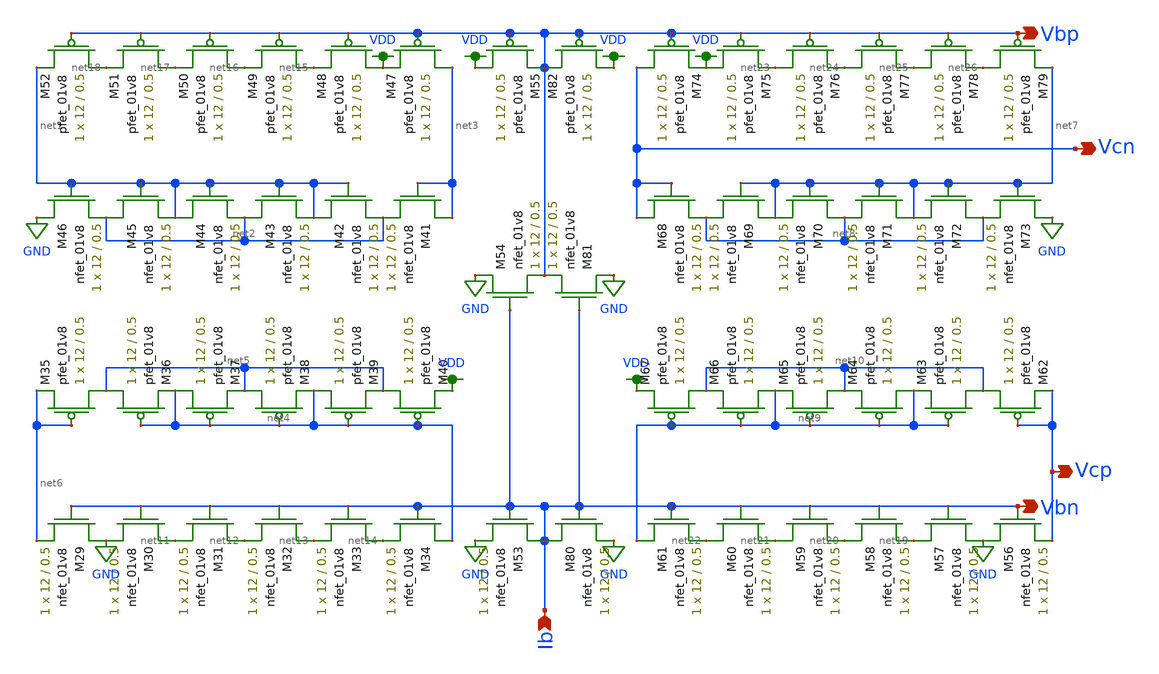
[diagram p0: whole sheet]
** sch_path: mp3/schematics/bias_lds.sch
**.subckt bias_lds Vbp Vbn Vcp Vcn Ib
*.opin Vbp
*.opin Vbn
*.opin Vcp
*.opin Vcn
*.ipin Ib
XM29 GND Vbn net6 GND sky130_fd_pr__nfet_01v8 L=0.5 W=12 nf=1 ad='int((nf+1)/2) * W/nf * 0.29' as='int((nf+2)/2) * W/nf * 0.29'
+ pd='2*int((nf+1)/2) * (W/nf + 0.29)' ps='2*int((nf+2)/2) * (W/nf + 0.29)' nrd='0.29 / W' nrs='0.29 / W'
+ sa=0 sb=0 sd=0 mult=1 m=1
XM30 net11 Vbn GND GND sky130_fd_pr__nfet_01v8 L=0.5 W=12 nf=1 ad='int((nf+1)/2) * W/nf * 0.29' as='int((nf+2)/2) * W/nf * 0.29'
+ pd='2*int((nf+1)/2) * (W/nf + 0.29)' ps='2*int((nf+2)/2) * (W/nf + 0.29)' nrd='0.29 / W' nrs='0.29 / W'
+ sa=0 sb=0 sd=0 mult=1 m=1
XM31 net12 Vbn net11 GND sky130_fd_pr__nfet_01v8 L=0.5 W=12 nf=1 ad='int((nf+1)/2) * W/nf * 0.29' as='int((nf+2)/2) * W/nf * 0.29'
+ pd='2*int((nf+1)/2) * (W/nf + 0.29)' ps='2*int((nf+2)/2) * (W/nf + 0.29)' nrd='0.29 / W' nrs='0.29 / W'
+ sa=0 sb=0 sd=0 mult=1 m=1
XM32 net13 Vbn net12 GND sky130_fd_pr__nfet_01v8 L=0.5 W=12 nf=1 ad='int((nf+1)/2) * W/nf * 0.29' as='int((nf+2)/2) * W/nf * 0.29'
+ pd='2*int((nf+1)/2) * (W/nf + 0.29)' ps='2*int((nf+2)/2) * (W/nf + 0.29)' nrd='0.29 / W' nrs='0.29 / W'
+ sa=0 sb=0 sd=0 mult=1 m=1
XM33 net14 Vbn net13 GND sky130_fd_pr__nfet_01v8 L=0.5 W=12 nf=1 ad='int((nf+1)/2) * W/nf * 0.29' as='int((nf+2)/2) * W/nf * 0.29'
+ pd='2*int((nf+1)/2) * (W/nf + 0.29)' ps='2*int((nf+2)/2) * (W/nf + 0.29)' nrd='0.29 / W' nrs='0.29 / W'
+ sa=0 sb=0 sd=0 mult=1 m=1
XM34 net4 Vbn net14 GND sky130_fd_pr__nfet_01v8 L=0.5 W=12 nf=1 ad='int((nf+1)/2) * W/nf * 0.29' as='int((nf+2)/2) * W/nf * 0.29'
+ pd='2*int((nf+1)/2) * (W/nf + 0.29)' ps='2*int((nf+2)/2) * (W/nf + 0.29)' nrd='0.29 / W' nrs='0.29 / W'
+ sa=0 sb=0 sd=0 mult=1 m=1
XM35 net5 net6 net6 VDD sky130_fd_pr__pfet_01v8 L=0.5 W=12 nf=1 ad='int((nf+1)/2) * W/nf * 0.29' as='int((nf+2)/2) * W/nf * 0.29'
+ pd='2*int((nf+1)/2) * (W/nf + 0.29)' ps='2*int((nf+2)/2) * (W/nf + 0.29)' nrd='0.29 / W' nrs='0.29 / W'
+ sa=0 sb=0 sd=0 mult=1 m=1
XM36 net5 net4 net4 VDD sky130_fd_pr__pfet_01v8 L=0.5 W=12 nf=1 ad='int((nf+1)/2) * W/nf * 0.29' as='int((nf+2)/2) * W/nf * 0.29'
+ pd='2*int((nf+1)/2) * (W/nf + 0.29)' ps='2*int((nf+2)/2) * (W/nf + 0.29)' nrd='0.29 / W' nrs='0.29 / W'
+ sa=0 sb=0 sd=0 mult=1 m=1
XM37 net4 net4 net5 VDD sky130_fd_pr__pfet_01v8 L=0.5 W=12 nf=1 ad='int((nf+1)/2) * W/nf * 0.29' as='int((nf+2)/2) * W/nf * 0.29'
+ pd='2*int((nf+1)/2) * (W/nf + 0.29)' ps='2*int((nf+2)/2) * (W/nf + 0.29)' nrd='0.29 / W' nrs='0.29 / W'
+ sa=0 sb=0 sd=0 mult=1 m=1
XM38 net5 net4 net4 VDD sky130_fd_pr__pfet_01v8 L=0.5 W=12 nf=1 ad='int((nf+1)/2) * W/nf * 0.29' as='int((nf+2)/2) * W/nf * 0.29'
+ pd='2*int((nf+1)/2) * (W/nf + 0.29)' ps='2*int((nf+2)/2) * (W/nf + 0.29)' nrd='0.29 / W' nrs='0.29 / W'
+ sa=0 sb=0 sd=0 mult=1 m=1
XM39 net4 net4 net5 VDD sky130_fd_pr__pfet_01v8 L=0.5 W=12 nf=1 ad='int((nf+1)/2) * W/nf * 0.29' as='int((nf+2)/2) * W/nf * 0.29'
+ pd='2*int((nf+1)/2) * (W/nf + 0.29)' ps='2*int((nf+2)/2) * (W/nf + 0.29)' nrd='0.29 / W' nrs='0.29 / W'
+ sa=0 sb=0 sd=0 mult=1 m=1
XM40 net5 net4 VDD VDD sky130_fd_pr__pfet_01v8 L=0.5 W=12 nf=1 ad='int((nf+1)/2) * W/nf * 0.29' as='int((nf+2)/2) * W/nf * 0.29'
+ pd='2*int((nf+1)/2) * (W/nf + 0.29)' ps='2*int((nf+2)/2) * (W/nf + 0.29)' nrd='0.29 / W' nrs='0.29 / W'
+ sa=0 sb=0 sd=0 mult=1 m=1
XM41 net3 net3 net2 GND sky130_fd_pr__nfet_01v8 L=0.5 W=12 nf=1 ad='int((nf+1)/2) * W/nf * 0.29' as='int((nf+2)/2) * W/nf * 0.29'
+ pd='2*int((nf+1)/2) * (W/nf + 0.29)' ps='2*int((nf+2)/2) * (W/nf + 0.29)' nrd='0.29 / W' nrs='0.29 / W'
+ sa=0 sb=0 sd=0 mult=1 m=1
XM42 net1 net1 net2 GND sky130_fd_pr__nfet_01v8 L=0.5 W=12 nf=1 ad='int((nf+1)/2) * W/nf * 0.29' as='int((nf+2)/2) * W/nf * 0.29'
+ pd='2*int((nf+1)/2) * (W/nf + 0.29)' ps='2*int((nf+2)/2) * (W/nf + 0.29)' nrd='0.29 / W' nrs='0.29 / W'
+ sa=0 sb=0 sd=0 mult=1 m=1
XM43 net2 net1 net1 GND sky130_fd_pr__nfet_01v8 L=0.5 W=12 nf=1 ad='int((nf+1)/2) * W/nf * 0.29' as='int((nf+2)/2) * W/nf * 0.29'
+ pd='2*int((nf+1)/2) * (W/nf + 0.29)' ps='2*int((nf+2)/2) * (W/nf + 0.29)' nrd='0.29 / W' nrs='0.29 / W'
+ sa=0 sb=0 sd=0 mult=1 m=1
XM44 net1 net1 net2 GND sky130_fd_pr__nfet_01v8 L=0.5 W=12 nf=1 ad='int((nf+1)/2) * W/nf * 0.29' as='int((nf+2)/2) * W/nf * 0.29'
+ pd='2*int((nf+1)/2) * (W/nf + 0.29)' ps='2*int((nf+2)/2) * (W/nf + 0.29)' nrd='0.29 / W' nrs='0.29 / W'
+ sa=0 sb=0 sd=0 mult=1 m=1
XM45 net2 net1 net1 GND sky130_fd_pr__nfet_01v8 L=0.5 W=12 nf=1 ad='int((nf+1)/2) * W/nf * 0.29' as='int((nf+2)/2) * W/nf * 0.29'
+ pd='2*int((nf+1)/2) * (W/nf + 0.29)' ps='2*int((nf+2)/2) * (W/nf + 0.29)' nrd='0.29 / W' nrs='0.29 / W'
+ sa=0 sb=0 sd=0 mult=1 m=1
XM46 GND net1 net2 GND sky130_fd_pr__nfet_01v8 L=0.5 W=12 nf=1 ad='int((nf+1)/2) * W/nf * 0.29' as='int((nf+2)/2) * W/nf * 0.29'
+ pd='2*int((nf+1)/2) * (W/nf + 0.29)' ps='2*int((nf+2)/2) * (W/nf + 0.29)' nrd='0.29 / W' nrs='0.29 / W'
+ sa=0 sb=0 sd=0 mult=1 m=1
XM47 net3 Vbp VDD VDD sky130_fd_pr__pfet_01v8 L=0.5 W=12 nf=1 ad='int((nf+1)/2) * W/nf * 0.29' as='int((nf+2)/2) * W/nf * 0.29'
+ pd='2*int((nf+1)/2) * (W/nf + 0.29)' ps='2*int((nf+2)/2) * (W/nf + 0.29)' nrd='0.29 / W' nrs='0.29 / W'
+ sa=0 sb=0 sd=0 mult=1 m=1
XM48 VDD Vbp net15 VDD sky130_fd_pr__pfet_01v8 L=0.5 W=12 nf=1 ad='int((nf+1)/2) * W/nf * 0.29' as='int((nf+2)/2) * W/nf * 0.29'
+ pd='2*int((nf+1)/2) * (W/nf + 0.29)' ps='2*int((nf+2)/2) * (W/nf + 0.29)' nrd='0.29 / W' nrs='0.29 / W'
+ sa=0 sb=0 sd=0 mult=1 m=1
XM49 net15 Vbp net16 VDD sky130_fd_pr__pfet_01v8 L=0.5 W=12 nf=1 ad='int((nf+1)/2) * W/nf * 0.29' as='int((nf+2)/2) * W/nf * 0.29'
+ pd='2*int((nf+1)/2) * (W/nf + 0.29)' ps='2*int((nf+2)/2) * (W/nf + 0.29)' nrd='0.29 / W' nrs='0.29 / W'
+ sa=0 sb=0 sd=0 mult=1 m=1
XM50 net16 Vbp net17 VDD sky130_fd_pr__pfet_01v8 L=0.5 W=12 nf=1 ad='int((nf+1)/2) * W/nf * 0.29' as='int((nf+2)/2) * W/nf * 0.29'
+ pd='2*int((nf+1)/2) * (W/nf + 0.29)' ps='2*int((nf+2)/2) * (W/nf + 0.29)' nrd='0.29 / W' nrs='0.29 / W'
+ sa=0 sb=0 sd=0 mult=1 m=1
XM51 net17 Vbp net18 VDD sky130_fd_pr__pfet_01v8 L=0.5 W=12 nf=1 ad='int((nf+1)/2) * W/nf * 0.29' as='int((nf+2)/2) * W/nf * 0.29'
+ pd='2*int((nf+1)/2) * (W/nf + 0.29)' ps='2*int((nf+2)/2) * (W/nf + 0.29)' nrd='0.29 / W' nrs='0.29 / W'
+ sa=0 sb=0 sd=0 mult=1 m=1
XM52 net18 Vbp net1 VDD sky130_fd_pr__pfet_01v8 L=0.5 W=12 nf=1 ad='int((nf+1)/2) * W/nf * 0.29' as='int((nf+2)/2) * W/nf * 0.29'
+ pd='2*int((nf+1)/2) * (W/nf + 0.29)' ps='2*int((nf+2)/2) * (W/nf + 0.29)' nrd='0.29 / W' nrs='0.29 / W'
+ sa=0 sb=0 sd=0 mult=1 m=1
XM53 Vbn Vbn GND GND sky130_fd_pr__nfet_01v8 L=0.5 W=12 nf=1 ad='int((nf+1)/2) * W/nf * 0.29' as='int((nf+2)/2) * W/nf * 0.29'
+ pd='2*int((nf+1)/2) * (W/nf + 0.29)' ps='2*int((nf+2)/2) * (W/nf + 0.29)' nrd='0.29 / W' nrs='0.29 / W'
+ sa=0 sb=0 sd=0 mult=1 m=1
XM54 GND Vbn Vbp GND sky130_fd_pr__nfet_01v8 L=0.5 W=12 nf=1 ad='int((nf+1)/2) * W/nf * 0.29' as='int((nf+2)/2) * W/nf * 0.29'
+ pd='2*int((nf+1)/2) * (W/nf + 0.29)' ps='2*int((nf+2)/2) * (W/nf + 0.29)' nrd='0.29 / W' nrs='0.29 / W'
+ sa=0 sb=0 sd=0 mult=1 m=1
XM55 VDD Vbp Vbp VDD sky130_fd_pr__pfet_01v8 L=0.5 W=12 nf=1 ad='int((nf+1)/2) * W/nf * 0.29' as='int((nf+2)/2) * W/nf * 0.29'
+ pd='2*int((nf+1)/2) * (W/nf + 0.29)' ps='2*int((nf+2)/2) * (W/nf + 0.29)' nrd='0.29 / W' nrs='0.29 / W'
+ sa=0 sb=0 sd=0 mult=1 m=1
XM56 GND Vbn Vcp GND sky130_fd_pr__nfet_01v8 L=0.5 W=12 nf=1 ad='int((nf+1)/2) * W/nf * 0.29' as='int((nf+2)/2) * W/nf * 0.29'
+ pd='2*int((nf+1)/2) * (W/nf + 0.29)' ps='2*int((nf+2)/2) * (W/nf + 0.29)' nrd='0.29 / W' nrs='0.29 / W'
+ sa=0 sb=0 sd=0 mult=1 m=1
XM57 net19 Vbn GND GND sky130_fd_pr__nfet_01v8 L=0.5 W=12 nf=1 ad='int((nf+1)/2) * W/nf * 0.29' as='int((nf+2)/2) * W/nf * 0.29'
+ pd='2*int((nf+1)/2) * (W/nf + 0.29)' ps='2*int((nf+2)/2) * (W/nf + 0.29)' nrd='0.29 / W' nrs='0.29 / W'
+ sa=0 sb=0 sd=0 mult=1 m=1
XM58 net20 Vbn net19 GND sky130_fd_pr__nfet_01v8 L=0.5 W=12 nf=1 ad='int((nf+1)/2) * W/nf * 0.29' as='int((nf+2)/2) * W/nf * 0.29'
+ pd='2*int((nf+1)/2) * (W/nf + 0.29)' ps='2*int((nf+2)/2) * (W/nf + 0.29)' nrd='0.29 / W' nrs='0.29 / W'
+ sa=0 sb=0 sd=0 mult=1 m=1
XM59 net21 Vbn net20 GND sky130_fd_pr__nfet_01v8 L=0.5 W=12 nf=1 ad='int((nf+1)/2) * W/nf * 0.29' as='int((nf+2)/2) * W/nf * 0.29'
+ pd='2*int((nf+1)/2) * (W/nf + 0.29)' ps='2*int((nf+2)/2) * (W/nf + 0.29)' nrd='0.29 / W' nrs='0.29 / W'
+ sa=0 sb=0 sd=0 mult=1 m=1
XM60 net22 Vbn net21 GND sky130_fd_pr__nfet_01v8 L=0.5 W=12 nf=1 ad='int((nf+1)/2) * W/nf * 0.29' as='int((nf+2)/2) * W/nf * 0.29'
+ pd='2*int((nf+1)/2) * (W/nf + 0.29)' ps='2*int((nf+2)/2) * (W/nf + 0.29)' nrd='0.29 / W' nrs='0.29 / W'
+ sa=0 sb=0 sd=0 mult=1 m=1
XM61 net9 Vbn net22 GND sky130_fd_pr__nfet_01v8 L=0.5 W=12 nf=1 ad='int((nf+1)/2) * W/nf * 0.29' as='int((nf+2)/2) * W/nf * 0.29'
+ pd='2*int((nf+1)/2) * (W/nf + 0.29)' ps='2*int((nf+2)/2) * (W/nf + 0.29)' nrd='0.29 / W' nrs='0.29 / W'
+ sa=0 sb=0 sd=0 mult=1 m=1
XM62 net10 Vcp Vcp VDD sky130_fd_pr__pfet_01v8 L=0.5 W=12 nf=1 ad='int((nf+1)/2) * W/nf * 0.29' as='int((nf+2)/2) * W/nf * 0.29'
+ pd='2*int((nf+1)/2) * (W/nf + 0.29)' ps='2*int((nf+2)/2) * (W/nf + 0.29)' nrd='0.29 / W' nrs='0.29 / W'
+ sa=0 sb=0 sd=0 mult=1 m=1
XM63 net10 net9 net9 VDD sky130_fd_pr__pfet_01v8 L=0.5 W=12 nf=1 ad='int((nf+1)/2) * W/nf * 0.29' as='int((nf+2)/2) * W/nf * 0.29'
+ pd='2*int((nf+1)/2) * (W/nf + 0.29)' ps='2*int((nf+2)/2) * (W/nf + 0.29)' nrd='0.29 / W' nrs='0.29 / W'
+ sa=0 sb=0 sd=0 mult=1 m=1
XM64 net9 net9 net10 VDD sky130_fd_pr__pfet_01v8 L=0.5 W=12 nf=1 ad='int((nf+1)/2) * W/nf * 0.29' as='int((nf+2)/2) * W/nf * 0.29'
+ pd='2*int((nf+1)/2) * (W/nf + 0.29)' ps='2*int((nf+2)/2) * (W/nf + 0.29)' nrd='0.29 / W' nrs='0.29 / W'
+ sa=0 sb=0 sd=0 mult=1 m=1
XM65 net10 net9 net9 VDD sky130_fd_pr__pfet_01v8 L=0.5 W=12 nf=1 ad='int((nf+1)/2) * W/nf * 0.29' as='int((nf+2)/2) * W/nf * 0.29'
+ pd='2*int((nf+1)/2) * (W/nf + 0.29)' ps='2*int((nf+2)/2) * (W/nf + 0.29)' nrd='0.29 / W' nrs='0.29 / W'
+ sa=0 sb=0 sd=0 mult=1 m=1
XM66 net9 net9 net10 VDD sky130_fd_pr__pfet_01v8 L=0.5 W=12 nf=1 ad='int((nf+1)/2) * W/nf * 0.29' as='int((nf+2)/2) * W/nf * 0.29'
+ pd='2*int((nf+1)/2) * (W/nf + 0.29)' ps='2*int((nf+2)/2) * (W/nf + 0.29)' nrd='0.29 / W' nrs='0.29 / W'
+ sa=0 sb=0 sd=0 mult=1 m=1
XM67 net10 net9 VDD VDD sky130_fd_pr__pfet_01v8 L=0.5 W=12 nf=1 ad='int((nf+1)/2) * W/nf * 0.29' as='int((nf+2)/2) * W/nf * 0.29'
+ pd='2*int((nf+1)/2) * (W/nf + 0.29)' ps='2*int((nf+2)/2) * (W/nf + 0.29)' nrd='0.29 / W' nrs='0.29 / W'
+ sa=0 sb=0 sd=0 mult=1 m=1
XM68 Vcn Vcn net8 GND sky130_fd_pr__nfet_01v8 L=0.5 W=12 nf=1 ad='int((nf+1)/2) * W/nf * 0.29' as='int((nf+2)/2) * W/nf * 0.29'
+ pd='2*int((nf+1)/2) * (W/nf + 0.29)' ps='2*int((nf+2)/2) * (W/nf + 0.29)' nrd='0.29 / W' nrs='0.29 / W'
+ sa=0 sb=0 sd=0 mult=1 m=1
XM69 net7 net7 net8 GND sky130_fd_pr__nfet_01v8 L=0.5 W=12 nf=1 ad='int((nf+1)/2) * W/nf * 0.29' as='int((nf+2)/2) * W/nf * 0.29'
+ pd='2*int((nf+1)/2) * (W/nf + 0.29)' ps='2*int((nf+2)/2) * (W/nf + 0.29)' nrd='0.29 / W' nrs='0.29 / W'
+ sa=0 sb=0 sd=0 mult=1 m=1
XM70 net8 net7 net7 GND sky130_fd_pr__nfet_01v8 L=0.5 W=12 nf=1 ad='int((nf+1)/2) * W/nf * 0.29' as='int((nf+2)/2) * W/nf * 0.29'
+ pd='2*int((nf+1)/2) * (W/nf + 0.29)' ps='2*int((nf+2)/2) * (W/nf + 0.29)' nrd='0.29 / W' nrs='0.29 / W'
+ sa=0 sb=0 sd=0 mult=1 m=1
XM71 net7 net7 net8 GND sky130_fd_pr__nfet_01v8 L=0.5 W=12 nf=1 ad='int((nf+1)/2) * W/nf * 0.29' as='int((nf+2)/2) * W/nf * 0.29'
+ pd='2*int((nf+1)/2) * (W/nf + 0.29)' ps='2*int((nf+2)/2) * (W/nf + 0.29)' nrd='0.29 / W' nrs='0.29 / W'
+ sa=0 sb=0 sd=0 mult=1 m=1
XM72 net8 net7 net7 GND sky130_fd_pr__nfet_01v8 L=0.5 W=12 nf=1 ad='int((nf+1)/2) * W/nf * 0.29' as='int((nf+2)/2) * W/nf * 0.29'
+ pd='2*int((nf+1)/2) * (W/nf + 0.29)' ps='2*int((nf+2)/2) * (W/nf + 0.29)' nrd='0.29 / W' nrs='0.29 / W'
+ sa=0 sb=0 sd=0 mult=1 m=1
XM73 GND net7 net8 GND sky130_fd_pr__nfet_01v8 L=0.5 W=12 nf=1 ad='int((nf+1)/2) * W/nf * 0.29' as='int((nf+2)/2) * W/nf * 0.29'
+ pd='2*int((nf+1)/2) * (W/nf + 0.29)' ps='2*int((nf+2)/2) * (W/nf + 0.29)' nrd='0.29 / W' nrs='0.29 / W'
+ sa=0 sb=0 sd=0 mult=1 m=1
XM74 Vcn Vbp VDD VDD sky130_fd_pr__pfet_01v8 L=0.5 W=12 nf=1 ad='int((nf+1)/2) * W/nf * 0.29' as='int((nf+2)/2) * W/nf * 0.29'
+ pd='2*int((nf+1)/2) * (W/nf + 0.29)' ps='2*int((nf+2)/2) * (W/nf + 0.29)' nrd='0.29 / W' nrs='0.29 / W'
+ sa=0 sb=0 sd=0 mult=1 m=1
XM75 VDD Vbp net23 VDD sky130_fd_pr__pfet_01v8 L=0.5 W=12 nf=1 ad='int((nf+1)/2) * W/nf * 0.29' as='int((nf+2)/2) * W/nf * 0.29'
+ pd='2*int((nf+1)/2) * (W/nf + 0.29)' ps='2*int((nf+2)/2) * (W/nf + 0.29)' nrd='0.29 / W' nrs='0.29 / W'
+ sa=0 sb=0 sd=0 mult=1 m=1
XM76 net23 Vbp net24 VDD sky130_fd_pr__pfet_01v8 L=0.5 W=12 nf=1 ad='int((nf+1)/2) * W/nf * 0.29' as='int((nf+2)/2) * W/nf * 0.29'
+ pd='2*int((nf+1)/2) * (W/nf + 0.29)' ps='2*int((nf+2)/2) * (W/nf + 0.29)' nrd='0.29 / W' nrs='0.29 / W'
+ sa=0 sb=0 sd=0 mult=1 m=1
XM77 net24 Vbp net25 VDD sky130_fd_pr__pfet_01v8 L=0.5 W=12 nf=1 ad='int((nf+1)/2) * W/nf * 0.29' as='int((nf+2)/2) * W/nf * 0.29'
+ pd='2*int((nf+1)/2) * (W/nf + 0.29)' ps='2*int((nf+2)/2) * (W/nf + 0.29)' nrd='0.29 / W' nrs='0.29 / W'
+ sa=0 sb=0 sd=0 mult=1 m=1
XM78 net25 Vbp net26 VDD sky130_fd_pr__pfet_01v8 L=0.5 W=12 nf=1 ad='int((nf+1)/2) * W/nf * 0.29' as='int((nf+2)/2) * W/nf * 0.29'
+ pd='2*int((nf+1)/2) * (W/nf + 0.29)' ps='2*int((nf+2)/2) * (W/nf + 0.29)' nrd='0.29 / W' nrs='0.29 / W'
+ sa=0 sb=0 sd=0 mult=1 m=1
XM79 net26 Vbp net7 VDD sky130_fd_pr__pfet_01v8 L=0.5 W=12 nf=1 ad='int((nf+1)/2) * W/nf * 0.29' as='int((nf+2)/2) * W/nf * 0.29'
+ pd='2*int((nf+1)/2) * (W/nf + 0.29)' ps='2*int((nf+2)/2) * (W/nf + 0.29)' nrd='0.29 / W' nrs='0.29 / W'
+ sa=0 sb=0 sd=0 mult=1 m=1
XM80 Vbn Vbn GND GND sky130_fd_pr__nfet_01v8 L=0.5 W=12 nf=1 ad='int((nf+1)/2) * W/nf * 0.29' as='int((nf+2)/2) * W/nf * 0.29'
+ pd='2*int((nf+1)/2) * (W/nf + 0.29)' ps='2*int((nf+2)/2) * (W/nf + 0.29)' nrd='0.29 / W' nrs='0.29 / W'
+ sa=0 sb=0 sd=0 mult=1 m=1
XM81 GND Vbn Vbp GND sky130_fd_pr__nfet_01v8 L=0.5 W=12 nf=1 ad='int((nf+1)/2) * W/nf * 0.29' as='int((nf+2)/2) * W/nf * 0.29'
+ pd='2*int((nf+1)/2) * (W/nf + 0.29)' ps='2*int((nf+2)/2) * (W/nf + 0.29)' nrd='0.29 / W' nrs='0.29 / W'
+ sa=0 sb=0 sd=0 mult=1 m=1
XM82 VDD Vbp Vbp VDD sky130_fd_pr__pfet_01v8 L=0.5 W=12 nf=1 ad='int((nf+1)/2) * W/nf * 0.29' as='int((nf+2)/2) * W/nf * 0.29'
+ pd='2*int((nf+1)/2) * (W/nf + 0.29)' ps='2*int((nf+2)/2) * (W/nf + 0.29)' nrd='0.29 / W' nrs='0.29 / W'
+ sa=0 sb=0 sd=0 mult=1 m=1
**.ends
.GLOBAL GND
.GLOBAL VDD
.end
